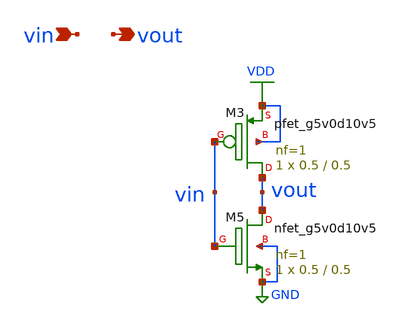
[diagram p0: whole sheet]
** sch_path: schematics/inverter.sch
**.subckt inverter vin vout
*.ipin vin
*.opin vout
XM3 vout vin VDD VDD sky130_fd_pr__pfet_g5v0d10v5 L=0.5 W=0.5 nf=1 ad='int((nf+1)/2) * W/nf * 0.29' as='int((nf+2)/2) * W/nf * 0.29'
+ pd='2*int((nf+1)/2) * (W/nf + 0.29)' ps='2*int((nf+2)/2) * (W/nf + 0.29)' nrd='0.29 / W' nrs='0.29 / W'
+ sa=0 sb=0 sd=0 mult=1 m=1
XM5 vout vin GND GND sky130_fd_pr__nfet_g5v0d10v5 L=0.5 W=0.5 nf=1 ad='int((nf+1)/2) * W/nf * 0.29' as='int((nf+2)/2) * W/nf * 0.29'
+ pd='2*int((nf+1)/2) * (W/nf + 0.29)' ps='2*int((nf+2)/2) * (W/nf + 0.29)' nrd='0.29 / W' nrs='0.29 / W'
+ sa=0 sb=0 sd=0 mult=1 m=1
**.ends
.GLOBAL GND
.GLOBAL VDD
.end
